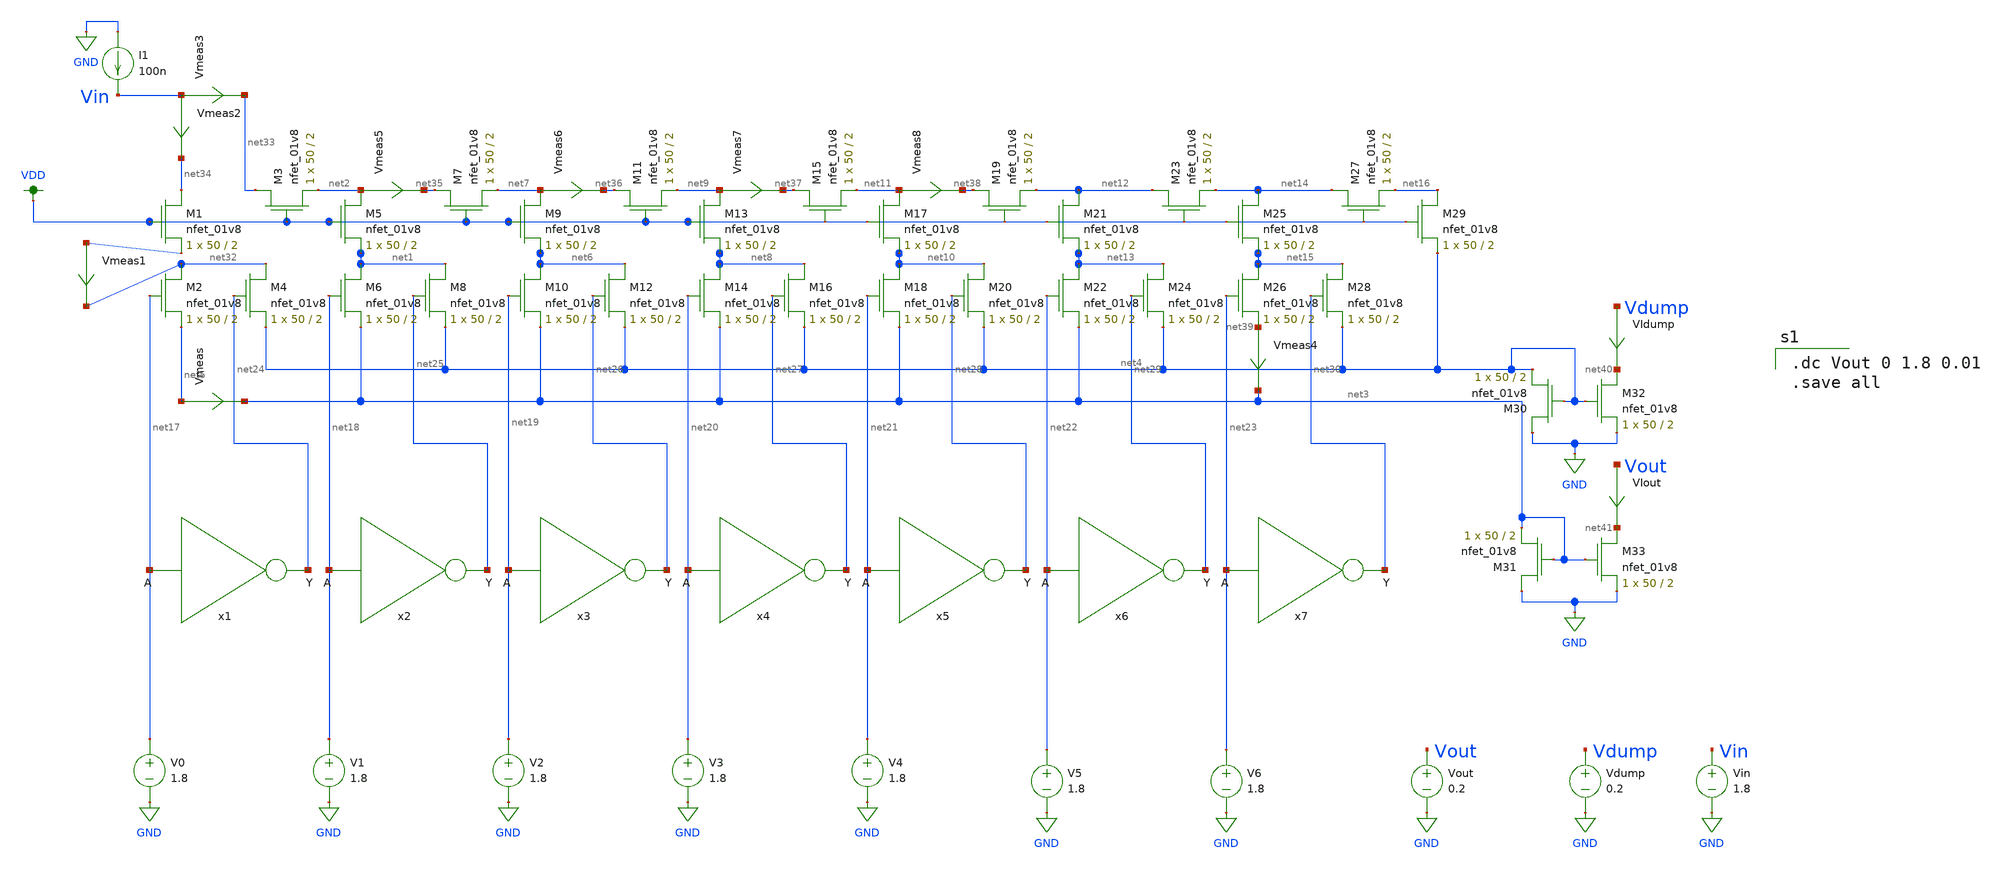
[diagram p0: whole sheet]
** sch_path: xschem/ladder_lauren.sch
**.subckt ladder_lauren
XM1 net34 VDD net31 GND sky130_fd_pr__nfet_01v8 L=2 W=50 nf=1 ad='int((nf+1)/2) * W/nf * 0.29' as='int((nf+2)/2) * W/nf * 0.29'
+ pd='2*int((nf+1)/2) * (W/nf + 0.29)' ps='2*int((nf+2)/2) * (W/nf + 0.29)' nrd='0.29 / W' nrs='0.29 / W'
+ sa=0 sb=0 sd=0 mult=1 m=1
XM3 net33 VDD net2 GND sky130_fd_pr__nfet_01v8 L=2 W=50 nf=1 ad='int((nf+1)/2) * W/nf * 0.29' as='int((nf+2)/2) * W/nf * 0.29'
+ pd='2*int((nf+1)/2) * (W/nf + 0.29)' ps='2*int((nf+2)/2) * (W/nf + 0.29)' nrd='0.29 / W' nrs='0.29 / W'
+ sa=0 sb=0 sd=0 mult=1 m=1
XM5 net2 VDD net1 GND sky130_fd_pr__nfet_01v8 L=2 W=50 nf=1 ad='int((nf+1)/2) * W/nf * 0.29' as='int((nf+2)/2) * W/nf * 0.29'
+ pd='2*int((nf+1)/2) * (W/nf + 0.29)' ps='2*int((nf+2)/2) * (W/nf + 0.29)' nrd='0.29 / W' nrs='0.29 / W'
+ sa=0 sb=0 sd=0 mult=1 m=1
XM7 net35 VDD net7 GND sky130_fd_pr__nfet_01v8 L=2 W=50 nf=1 ad='int((nf+1)/2) * W/nf * 0.29' as='int((nf+2)/2) * W/nf * 0.29'
+ pd='2*int((nf+1)/2) * (W/nf + 0.29)' ps='2*int((nf+2)/2) * (W/nf + 0.29)' nrd='0.29 / W' nrs='0.29 / W'
+ sa=0 sb=0 sd=0 mult=1 m=1
XM6 net1 net18 net3 GND sky130_fd_pr__nfet_01v8 L=2 W=50 nf=1 ad='int((nf+1)/2) * W/nf * 0.29' as='int((nf+2)/2) * W/nf * 0.29'
+ pd='2*int((nf+1)/2) * (W/nf + 0.29)' ps='2*int((nf+2)/2) * (W/nf + 0.29)' nrd='0.29 / W' nrs='0.29 / W'
+ sa=0 sb=0 sd=0 mult=1 m=1
XM8 net1 net25 net4 GND sky130_fd_pr__nfet_01v8 L=2 W=50 nf=1 ad='int((nf+1)/2) * W/nf * 0.29' as='int((nf+2)/2) * W/nf * 0.29'
+ pd='2*int((nf+1)/2) * (W/nf + 0.29)' ps='2*int((nf+2)/2) * (W/nf + 0.29)' nrd='0.29 / W' nrs='0.29 / W'
+ sa=0 sb=0 sd=0 mult=1 m=1
XM2 net32 net17 net5 GND sky130_fd_pr__nfet_01v8 L=2 W=50 nf=1 ad='int((nf+1)/2) * W/nf * 0.29' as='int((nf+2)/2) * W/nf * 0.29'
+ pd='2*int((nf+1)/2) * (W/nf + 0.29)' ps='2*int((nf+2)/2) * (W/nf + 0.29)' nrd='0.29 / W' nrs='0.29 / W'
+ sa=0 sb=0 sd=0 mult=1 m=1
XM4 net32 net24 net4 GND sky130_fd_pr__nfet_01v8 L=2 W=50 nf=1 ad='int((nf+1)/2) * W/nf * 0.29' as='int((nf+2)/2) * W/nf * 0.29'
+ pd='2*int((nf+1)/2) * (W/nf + 0.29)' ps='2*int((nf+2)/2) * (W/nf + 0.29)' nrd='0.29 / W' nrs='0.29 / W'
+ sa=0 sb=0 sd=0 mult=1 m=1
XM9 net7 VDD net6 GND sky130_fd_pr__nfet_01v8 L=2 W=50 nf=1 ad='int((nf+1)/2) * W/nf * 0.29' as='int((nf+2)/2) * W/nf * 0.29'
+ pd='2*int((nf+1)/2) * (W/nf + 0.29)' ps='2*int((nf+2)/2) * (W/nf + 0.29)' nrd='0.29 / W' nrs='0.29 / W'
+ sa=0 sb=0 sd=0 mult=1 m=1
XM11 net36 VDD net9 GND sky130_fd_pr__nfet_01v8 L=2 W=50 nf=1 ad='int((nf+1)/2) * W/nf * 0.29' as='int((nf+2)/2) * W/nf * 0.29'
+ pd='2*int((nf+1)/2) * (W/nf + 0.29)' ps='2*int((nf+2)/2) * (W/nf + 0.29)' nrd='0.29 / W' nrs='0.29 / W'
+ sa=0 sb=0 sd=0 mult=1 m=1
XM10 net6 net19 net3 GND sky130_fd_pr__nfet_01v8 L=2 W=50 nf=1 ad='int((nf+1)/2) * W/nf * 0.29' as='int((nf+2)/2) * W/nf * 0.29'
+ pd='2*int((nf+1)/2) * (W/nf + 0.29)' ps='2*int((nf+2)/2) * (W/nf + 0.29)' nrd='0.29 / W' nrs='0.29 / W'
+ sa=0 sb=0 sd=0 mult=1 m=1
XM12 net6 net26 net4 GND sky130_fd_pr__nfet_01v8 L=2 W=50 nf=1 ad='int((nf+1)/2) * W/nf * 0.29' as='int((nf+2)/2) * W/nf * 0.29'
+ pd='2*int((nf+1)/2) * (W/nf + 0.29)' ps='2*int((nf+2)/2) * (W/nf + 0.29)' nrd='0.29 / W' nrs='0.29 / W'
+ sa=0 sb=0 sd=0 mult=1 m=1
XM13 net9 VDD net8 GND sky130_fd_pr__nfet_01v8 L=2 W=50 nf=1 ad='int((nf+1)/2) * W/nf * 0.29' as='int((nf+2)/2) * W/nf * 0.29'
+ pd='2*int((nf+1)/2) * (W/nf + 0.29)' ps='2*int((nf+2)/2) * (W/nf + 0.29)' nrd='0.29 / W' nrs='0.29 / W'
+ sa=0 sb=0 sd=0 mult=1 m=1
XM15 net37 VDD net11 GND sky130_fd_pr__nfet_01v8 L=2 W=50 nf=1 ad='int((nf+1)/2) * W/nf * 0.29' as='int((nf+2)/2) * W/nf * 0.29'
+ pd='2*int((nf+1)/2) * (W/nf + 0.29)' ps='2*int((nf+2)/2) * (W/nf + 0.29)' nrd='0.29 / W' nrs='0.29 / W'
+ sa=0 sb=0 sd=0 mult=1 m=1
XM14 net8 net20 net3 GND sky130_fd_pr__nfet_01v8 L=2 W=50 nf=1 ad='int((nf+1)/2) * W/nf * 0.29' as='int((nf+2)/2) * W/nf * 0.29'
+ pd='2*int((nf+1)/2) * (W/nf + 0.29)' ps='2*int((nf+2)/2) * (W/nf + 0.29)' nrd='0.29 / W' nrs='0.29 / W'
+ sa=0 sb=0 sd=0 mult=1 m=1
XM16 net8 net27 net4 GND sky130_fd_pr__nfet_01v8 L=2 W=50 nf=1 ad='int((nf+1)/2) * W/nf * 0.29' as='int((nf+2)/2) * W/nf * 0.29'
+ pd='2*int((nf+1)/2) * (W/nf + 0.29)' ps='2*int((nf+2)/2) * (W/nf + 0.29)' nrd='0.29 / W' nrs='0.29 / W'
+ sa=0 sb=0 sd=0 mult=1 m=1
XM17 net11 VDD net10 GND sky130_fd_pr__nfet_01v8 L=2 W=50 nf=1 ad='int((nf+1)/2) * W/nf * 0.29' as='int((nf+2)/2) * W/nf * 0.29'
+ pd='2*int((nf+1)/2) * (W/nf + 0.29)' ps='2*int((nf+2)/2) * (W/nf + 0.29)' nrd='0.29 / W' nrs='0.29 / W'
+ sa=0 sb=0 sd=0 mult=1 m=1
XM19 net38 VDD net12 GND sky130_fd_pr__nfet_01v8 L=2 W=50 nf=1 ad='int((nf+1)/2) * W/nf * 0.29' as='int((nf+2)/2) * W/nf * 0.29'
+ pd='2*int((nf+1)/2) * (W/nf + 0.29)' ps='2*int((nf+2)/2) * (W/nf + 0.29)' nrd='0.29 / W' nrs='0.29 / W'
+ sa=0 sb=0 sd=0 mult=1 m=1
XM18 net10 net21 net3 GND sky130_fd_pr__nfet_01v8 L=2 W=50 nf=1 ad='int((nf+1)/2) * W/nf * 0.29' as='int((nf+2)/2) * W/nf * 0.29'
+ pd='2*int((nf+1)/2) * (W/nf + 0.29)' ps='2*int((nf+2)/2) * (W/nf + 0.29)' nrd='0.29 / W' nrs='0.29 / W'
+ sa=0 sb=0 sd=0 mult=1 m=1
XM20 net10 net28 net4 GND sky130_fd_pr__nfet_01v8 L=2 W=50 nf=1 ad='int((nf+1)/2) * W/nf * 0.29' as='int((nf+2)/2) * W/nf * 0.29'
+ pd='2*int((nf+1)/2) * (W/nf + 0.29)' ps='2*int((nf+2)/2) * (W/nf + 0.29)' nrd='0.29 / W' nrs='0.29 / W'
+ sa=0 sb=0 sd=0 mult=1 m=1
XM21 net12 VDD net13 GND sky130_fd_pr__nfet_01v8 L=2 W=50 nf=1 ad='int((nf+1)/2) * W/nf * 0.29' as='int((nf+2)/2) * W/nf * 0.29'
+ pd='2*int((nf+1)/2) * (W/nf + 0.29)' ps='2*int((nf+2)/2) * (W/nf + 0.29)' nrd='0.29 / W' nrs='0.29 / W'
+ sa=0 sb=0 sd=0 mult=1 m=1
XM23 net12 VDD net14 GND sky130_fd_pr__nfet_01v8 L=2 W=50 nf=1 ad='int((nf+1)/2) * W/nf * 0.29' as='int((nf+2)/2) * W/nf * 0.29'
+ pd='2*int((nf+1)/2) * (W/nf + 0.29)' ps='2*int((nf+2)/2) * (W/nf + 0.29)' nrd='0.29 / W' nrs='0.29 / W'
+ sa=0 sb=0 sd=0 mult=1 m=1
XM22 net13 net22 net3 GND sky130_fd_pr__nfet_01v8 L=2 W=50 nf=1 ad='int((nf+1)/2) * W/nf * 0.29' as='int((nf+2)/2) * W/nf * 0.29'
+ pd='2*int((nf+1)/2) * (W/nf + 0.29)' ps='2*int((nf+2)/2) * (W/nf + 0.29)' nrd='0.29 / W' nrs='0.29 / W'
+ sa=0 sb=0 sd=0 mult=1 m=1
XM24 net13 net29 net4 GND sky130_fd_pr__nfet_01v8 L=2 W=50 nf=1 ad='int((nf+1)/2) * W/nf * 0.29' as='int((nf+2)/2) * W/nf * 0.29'
+ pd='2*int((nf+1)/2) * (W/nf + 0.29)' ps='2*int((nf+2)/2) * (W/nf + 0.29)' nrd='0.29 / W' nrs='0.29 / W'
+ sa=0 sb=0 sd=0 mult=1 m=1
XM25 net14 VDD net15 GND sky130_fd_pr__nfet_01v8 L=2 W=50 nf=1 ad='int((nf+1)/2) * W/nf * 0.29' as='int((nf+2)/2) * W/nf * 0.29'
+ pd='2*int((nf+1)/2) * (W/nf + 0.29)' ps='2*int((nf+2)/2) * (W/nf + 0.29)' nrd='0.29 / W' nrs='0.29 / W'
+ sa=0 sb=0 sd=0 mult=1 m=1
XM27 net14 VDD net16 GND sky130_fd_pr__nfet_01v8 L=2 W=50 nf=1 ad='int((nf+1)/2) * W/nf * 0.29' as='int((nf+2)/2) * W/nf * 0.29'
+ pd='2*int((nf+1)/2) * (W/nf + 0.29)' ps='2*int((nf+2)/2) * (W/nf + 0.29)' nrd='0.29 / W' nrs='0.29 / W'
+ sa=0 sb=0 sd=0 mult=1 m=1
XM26 net15 net23 net39 GND sky130_fd_pr__nfet_01v8 L=2 W=50 nf=1 ad='int((nf+1)/2) * W/nf * 0.29' as='int((nf+2)/2) * W/nf * 0.29'
+ pd='2*int((nf+1)/2) * (W/nf + 0.29)' ps='2*int((nf+2)/2) * (W/nf + 0.29)' nrd='0.29 / W' nrs='0.29 / W'
+ sa=0 sb=0 sd=0 mult=1 m=1
XM28 net15 net30 net4 GND sky130_fd_pr__nfet_01v8 L=2 W=50 nf=1 ad='int((nf+1)/2) * W/nf * 0.29' as='int((nf+2)/2) * W/nf * 0.29'
+ pd='2*int((nf+1)/2) * (W/nf + 0.29)' ps='2*int((nf+2)/2) * (W/nf + 0.29)' nrd='0.29 / W' nrs='0.29 / W'
+ sa=0 sb=0 sd=0 mult=1 m=1
XM29 net16 VDD net4 GND sky130_fd_pr__nfet_01v8 L=2 W=50 nf=1 ad='int((nf+1)/2) * W/nf * 0.29' as='int((nf+2)/2) * W/nf * 0.29'
+ pd='2*int((nf+1)/2) * (W/nf + 0.29)' ps='2*int((nf+2)/2) * (W/nf + 0.29)' nrd='0.29 / W' nrs='0.29 / W'
+ sa=0 sb=0 sd=0 mult=1 m=1
XM30 GND net4 net4 GND sky130_fd_pr__nfet_01v8 L=2 W=50 nf=1 ad='int((nf+1)/2) * W/nf * 0.29' as='int((nf+2)/2) * W/nf * 0.29'
+ pd='2*int((nf+1)/2) * (W/nf + 0.29)' ps='2*int((nf+2)/2) * (W/nf + 0.29)' nrd='0.29 / W' nrs='0.29 / W'
+ sa=0 sb=0 sd=0 mult=1 m=1
XM31 GND net3 net3 GND sky130_fd_pr__nfet_01v8 L=2 W=50 nf=1 ad='int((nf+1)/2) * W/nf * 0.29' as='int((nf+2)/2) * W/nf * 0.29'
+ pd='2*int((nf+1)/2) * (W/nf + 0.29)' ps='2*int((nf+2)/2) * (W/nf + 0.29)' nrd='0.29 / W' nrs='0.29 / W'
+ sa=0 sb=0 sd=0 mult=1 m=1
XM32 net40 net4 GND GND sky130_fd_pr__nfet_01v8 L=2 W=50 nf=1 ad='int((nf+1)/2) * W/nf * 0.29' as='int((nf+2)/2) * W/nf * 0.29'
+ pd='2*int((nf+1)/2) * (W/nf + 0.29)' ps='2*int((nf+2)/2) * (W/nf + 0.29)' nrd='0.29 / W' nrs='0.29 / W'
+ sa=0 sb=0 sd=0 mult=1 m=1
XM33 net41 net3 GND GND sky130_fd_pr__nfet_01v8 L=2 W=50 nf=1 ad='int((nf+1)/2) * W/nf * 0.29' as='int((nf+2)/2) * W/nf * 0.29'
+ pd='2*int((nf+1)/2) * (W/nf + 0.29)' ps='2*int((nf+2)/2) * (W/nf + 0.29)' nrd='0.29 / W' nrs='0.29 / W'
+ sa=0 sb=0 sd=0 mult=1 m=1
x1 net24 net17 inverter
x2 net25 net18 inverter
x3 net26 net19 inverter
x4 net27 net20 inverter
x5 net28 net21 inverter
x6 net29 net22 inverter
x7 net30 net23 inverter
I1 GND Vin 100n
V0 net17 GND 1.8
V1 net18 GND 1.8
V2 net19 GND 1.8
V3 net20 GND 1.8
V4 net21 GND 1.8
V5 net22 GND 1.8
V6 net23 GND 1.8
VIout Vout net41 0
.save i(viout)
VIdump Vdump net40 0
.save i(vidump)
Vout Vout GND 0.2
Vdump Vdump GND 0.2
Vmeas net5 net3 0
.save i(vmeas)
Vmeas1 net31 net32 0
.save i(vmeas1)
Vmeas3 Vin net33 0
.save i(vmeas3)
Vmeas4 net39 net3 0
.save i(vmeas4)
Vmeas5 net2 net35 0
.save i(vmeas5)
Vmeas6 net7 net36 0
.save i(vmeas6)
Vmeas7 net9 net37 0
.save i(vmeas7)
Vin Vin GND 1.8
Vmeas2 Vin net34 0
.save i(vmeas2)
Vmeas8 net11 net38 0
.save i(vmeas8)
**** begin user architecture code

.option wnflag=1
.lib ~/skywater/skywater-pdk/libraries/sky130_fd_pr_ngspice/latest/models/sky130.lib.spice tt


.dc Vout 0 1.8 0.01
.save all

**** end user architecture code
**.ends

* expanding   symbol:  ./inverter.sym # of pins=2
** sym_path: xschem/inverter.sym
** sch_path: xschem/inverter.sch
.subckt inverter Y A
*.ipin A
*.opin Y
XM1 Y A VDD VDD sky130_fd_pr__pfet_01v8 L=0.15 W=1 nf=1 ad='int((nf+1)/2) * W/nf * 0.29' as='int((nf+2)/2) * W/nf * 0.29'
+ pd='2*int((nf+1)/2) * (W/nf + 0.29)' ps='2*int((nf+2)/2) * (W/nf + 0.29)' nrd='0.29 / W' nrs='0.29 / W'
+ sa=0 sb=0 sd=0 mult=1 m=1
XM2 Y A GND GND sky130_fd_pr__nfet_01v8 L=0.15 W=1 nf=1 ad='int((nf+1)/2) * W/nf * 0.29' as='int((nf+2)/2) * W/nf * 0.29'
+ pd='2*int((nf+1)/2) * (W/nf + 0.29)' ps='2*int((nf+2)/2) * (W/nf + 0.29)' nrd='0.29 / W' nrs='0.29 / W'
+ sa=0 sb=0 sd=0 mult=1 m=1
.ends

.GLOBAL VDD
.GLOBAL GND
.end
